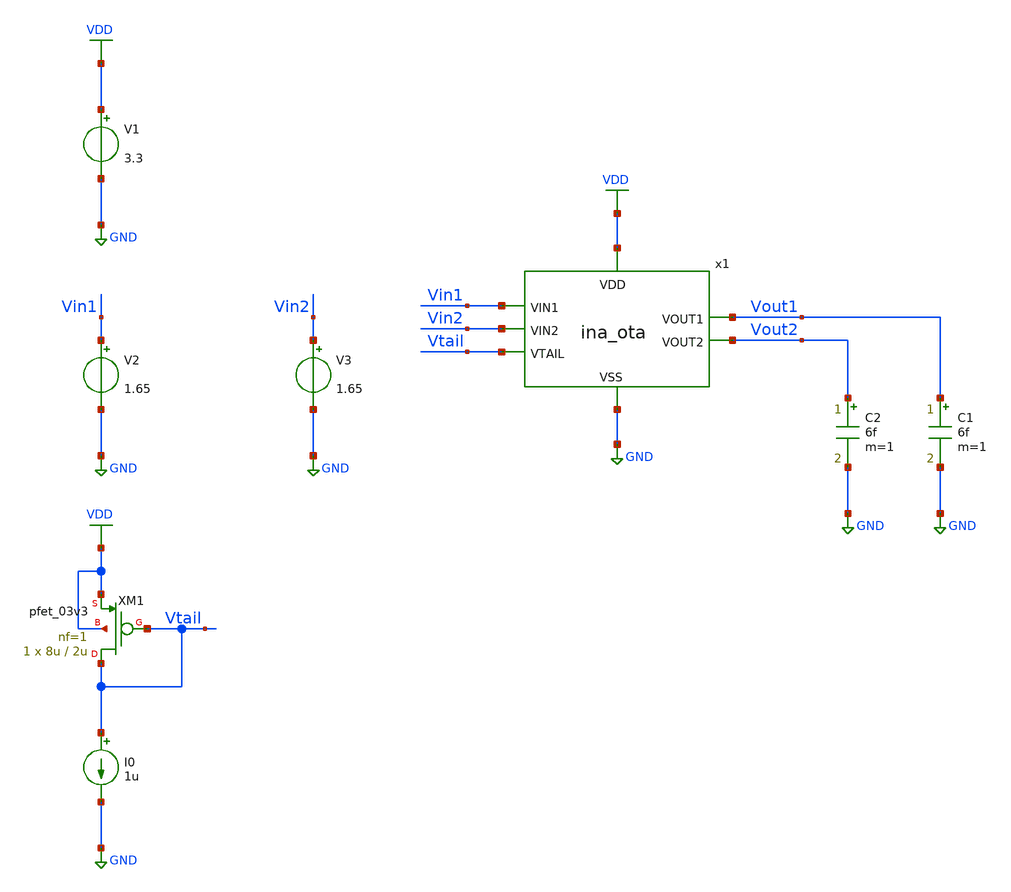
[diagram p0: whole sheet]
** sch_path: designs/libs/tb_ina/tb_ina_ota_noise/tb_ina_ota_noise.sch
**.subckt tb_ina_ota_noise
V1 VDD GND 3.3
V2 Vin1 GND 1.65
V3 Vin2 GND 1.65
XM1 Vtail Vtail VDD VDD pfet_03v3 L=2u W=8u nf=1 ad='int((nf+1)/2) * W/nf * 0.18u' as='int((nf+2)/2) * W/nf * 0.18u'
+ pd='2*int((nf+1)/2) * (W/nf + 0.18u)' ps='2*int((nf+2)/2) * (W/nf + 0.18u)' nrd='0.18u / W' nrs='0.18u / W'
+ sa=0 sb=0 sd=0 m=1
I0 Vtail GND 1u
x1 VDD Vtail Vin1 Vout2 Vout1 Vin2 GND ina_ota
C2 Vout2 GND 6f m=1
C1 Vout1 GND 6f m=1
**** begin user architecture code

.include $::180MCU_MODELS/design.ngspice
.lib $::180MCU_MODELS/sm141064.ngspice typical
.lib $::180MCU_MODELS/sm141064.ngspice cap_mim
.lib $::180MCU_MODELS/sm141064.ngspice moscap_typical
.lib $::180MCU_MODELS/sm141064.ngspice mimcap_typical
.lib $::180MCU_MODELS/sm141064.ngspice res_typical
* .lib $::180MCU_MODELS/sm141064.ngspice res_statistical
* ngspice commands




.control
save all

run
set color0 = white

*************************************
** PARAMETERS
*************************************

let Vdd  = 3.3
let Vcm  = 1.65
let Ibias = 2u

*************************************
** SOURCES
*************************************

alter @V1[DC] = $&Vdd
alter @V2[DC] = $&Vcm
alter @V3[DC] = $&Vcm
alter @V2[ACMAG] = 1
alter @V3[ACMAG] = 0
alter @I0[DC] = $&Ibias

*************************************
** NOISE SIMULATION
*************************************

op
noise v(Vout1) V2 dec 100 0.01 1G

*************************************
** PLOTS
*************************************

setplot noise1
plot onoise_spectrum
plot inoise_spectrum

*************************************
** MEASUREMENTS
*************************************

* Input-Referred Noise Density
let inoise_1Hz   = inoise_spectrum[200]
let inoise_10Hz  = inoise_spectrum[300]
let inoise_100Hz = inoise_spectrum[400]
print inoise_1Hz
print inoise_10Hz
print inoise_100Hz
* Output Noise Density
let onoise_1Hz = onoise_spectrum[200]
let onoise_10Hz = onoise_spectrum[300]
let onoise_100Hz = onoise_spectrum[400]
print onoise_1Hz
print onoise_10Hz
print onoise_100Hz

*************************************
** SAVE
*************************************

write tb_ina_ota_noise.raw

*************************************
** NOISE SIMULATION2
*************************************

noise v(Vout1) V2 dec 500 0.5 150

setplot noise4
* Integrated Input-Referred Noise (0.5 Hz - 150 Hz)
let inoise_rms = inoise_total
print inoise_rms
* Integrated Output Noise (0.5 Hz - 150 Hz)
let onoise_rms = onoise_total
print onoise_rms

.endc
* ngspice commands



**** end user architecture code
**.ends

* expanding   symbol:  libs/core_ina/ina_ota/ina_ota.sym # of pins=7
** sym_path: designs/libs/core_ina/ina_ota/ina_ota.sym
** sch_path: designs/libs/core_ina/ina_ota/ina_ota.sch
.subckt ina_ota VDD VTAIL VIN1 VOUT2 VOUT1 VIN2 VSS
*.ipin Vin1
*.ipin Vin2
*.ipin Vtail
*.ipin VSS
*.opin Vout1
*.ipin VDD
*.opin Vout2
XM2 net4 net4 VDD VDD pfet_03v3 L=6u W=0.65u nf=1 ad='int((nf+1)/2) * W/nf * 0.18u' as='int((nf+2)/2) * W/nf * 0.18u'
+ pd='2*int((nf+1)/2) * (W/nf + 0.18u)' ps='2*int((nf+2)/2) * (W/nf + 0.18u)' nrd='0.18u / W' nrs='0.18u / W'
+ sa=0 sb=0 sd=0 m=1
XM1 net3 Vtail VDD VDD pfet_03v3 L=2u W=8u nf=1 ad='int((nf+1)/2) * W/nf * 0.18u' as='int((nf+2)/2) * W/nf * 0.18u'
+ pd='2*int((nf+1)/2) * (W/nf + 0.18u)' ps='2*int((nf+2)/2) * (W/nf + 0.18u)' nrd='0.18u / W' nrs='0.18u / W'
+ sa=0 sb=0 sd=0 m=1
XM3 net5 net5 VDD VDD pfet_03v3 L=6u W=0.65u nf=1 ad='int((nf+1)/2) * W/nf * 0.18u' as='int((nf+2)/2) * W/nf * 0.18u'
+ pd='2*int((nf+1)/2) * (W/nf + 0.18u)' ps='2*int((nf+2)/2) * (W/nf + 0.18u)' nrd='0.18u / W' nrs='0.18u / W'
+ sa=0 sb=0 sd=0 m=1
XM4 net1 Vin1 net3 VDD pfet_03v3 L=0.28u W=15u nf=1 ad='int((nf+1)/2) * W/nf * 0.18u' as='int((nf+2)/2) * W/nf * 0.18u'
+ pd='2*int((nf+1)/2) * (W/nf + 0.18u)' ps='2*int((nf+2)/2) * (W/nf + 0.18u)' nrd='0.18u / W' nrs='0.18u / W'
+ sa=0 sb=0 sd=0 m=10
XM5 net2 Vin2 net3 VDD pfet_03v3 L=0.28u W=15u nf=1 ad='int((nf+1)/2) * W/nf * 0.18u' as='int((nf+2)/2) * W/nf * 0.18u'
+ pd='2*int((nf+1)/2) * (W/nf + 0.18u)' ps='2*int((nf+2)/2) * (W/nf + 0.18u)' nrd='0.18u / W' nrs='0.18u / W'
+ sa=0 sb=0 sd=0 m=10
XM6 net4 net1 VSS VSS nfet_03v3 L=6u W=1.8u nf=1 ad='int((nf+1)/2) * W/nf * 0.18u' as='int((nf+2)/2) * W/nf * 0.18u'
+ pd='2*int((nf+1)/2) * (W/nf + 0.18u)' ps='2*int((nf+2)/2) * (W/nf + 0.18u)' nrd='0.18u / W' nrs='0.18u / W'
+ sa=0 sb=0 sd=0 m=1
XM7 net5 net2 VSS VSS nfet_03v3 L=6u W=1.8u nf=1 ad='int((nf+1)/2) * W/nf * 0.18u' as='int((nf+2)/2) * W/nf * 0.18u'
+ pd='2*int((nf+1)/2) * (W/nf + 0.18u)' ps='2*int((nf+2)/2) * (W/nf + 0.18u)' nrd='0.18u / W' nrs='0.18u / W'
+ sa=0 sb=0 sd=0 m=1
XM8 net1 net1 VSS VSS nfet_03v3 L=6u W=1.8u nf=1 ad='int((nf+1)/2) * W/nf * 0.18u' as='int((nf+2)/2) * W/nf * 0.18u'
+ pd='2*int((nf+1)/2) * (W/nf + 0.18u)' ps='2*int((nf+2)/2) * (W/nf + 0.18u)' nrd='0.18u / W' nrs='0.18u / W'
+ sa=0 sb=0 sd=0 m=1
XM9 net2 net2 VSS VSS nfet_03v3 L=6u W=1.8u nf=1 ad='int((nf+1)/2) * W/nf * 0.18u' as='int((nf+2)/2) * W/nf * 0.18u'
+ pd='2*int((nf+1)/2) * (W/nf + 0.18u)' ps='2*int((nf+2)/2) * (W/nf + 0.18u)' nrd='0.18u / W' nrs='0.18u / W'
+ sa=0 sb=0 sd=0 m=1
XM10 Vout1 net4 VDD VDD pfet_03v3 L=6u W=0.65u nf=1 ad='int((nf+1)/2) * W/nf * 0.18u' as='int((nf+2)/2) * W/nf * 0.18u'
+ pd='2*int((nf+1)/2) * (W/nf + 0.18u)' ps='2*int((nf+2)/2) * (W/nf + 0.18u)' nrd='0.18u / W' nrs='0.18u / W'
+ sa=0 sb=0 sd=0 m=1
XM11 Vout1 net2 VSS VSS nfet_03v3 L=6u W=1.8u nf=1 ad='int((nf+1)/2) * W/nf * 0.18u' as='int((nf+2)/2) * W/nf * 0.18u'
+ pd='2*int((nf+1)/2) * (W/nf + 0.18u)' ps='2*int((nf+2)/2) * (W/nf + 0.18u)' nrd='0.18u / W' nrs='0.18u / W'
+ sa=0 sb=0 sd=0 m=1
XM12 Vout2 net1 VSS VSS nfet_03v3 L=6u W=1.8u nf=1 ad='int((nf+1)/2) * W/nf * 0.18u' as='int((nf+2)/2) * W/nf * 0.18u'
+ pd='2*int((nf+1)/2) * (W/nf + 0.18u)' ps='2*int((nf+2)/2) * (W/nf + 0.18u)' nrd='0.18u / W' nrs='0.18u / W'
+ sa=0 sb=0 sd=0 m=1
XM13 Vout2 net5 VDD VDD pfet_03v3 L=6u W=0.65u nf=1 ad='int((nf+1)/2) * W/nf * 0.18u' as='int((nf+2)/2) * W/nf * 0.18u'
+ pd='2*int((nf+1)/2) * (W/nf + 0.18u)' ps='2*int((nf+2)/2) * (W/nf + 0.18u)' nrd='0.18u / W' nrs='0.18u / W'
+ sa=0 sb=0 sd=0 m=1
.ends

.GLOBAL GND
.GLOBAL VDD
.end
